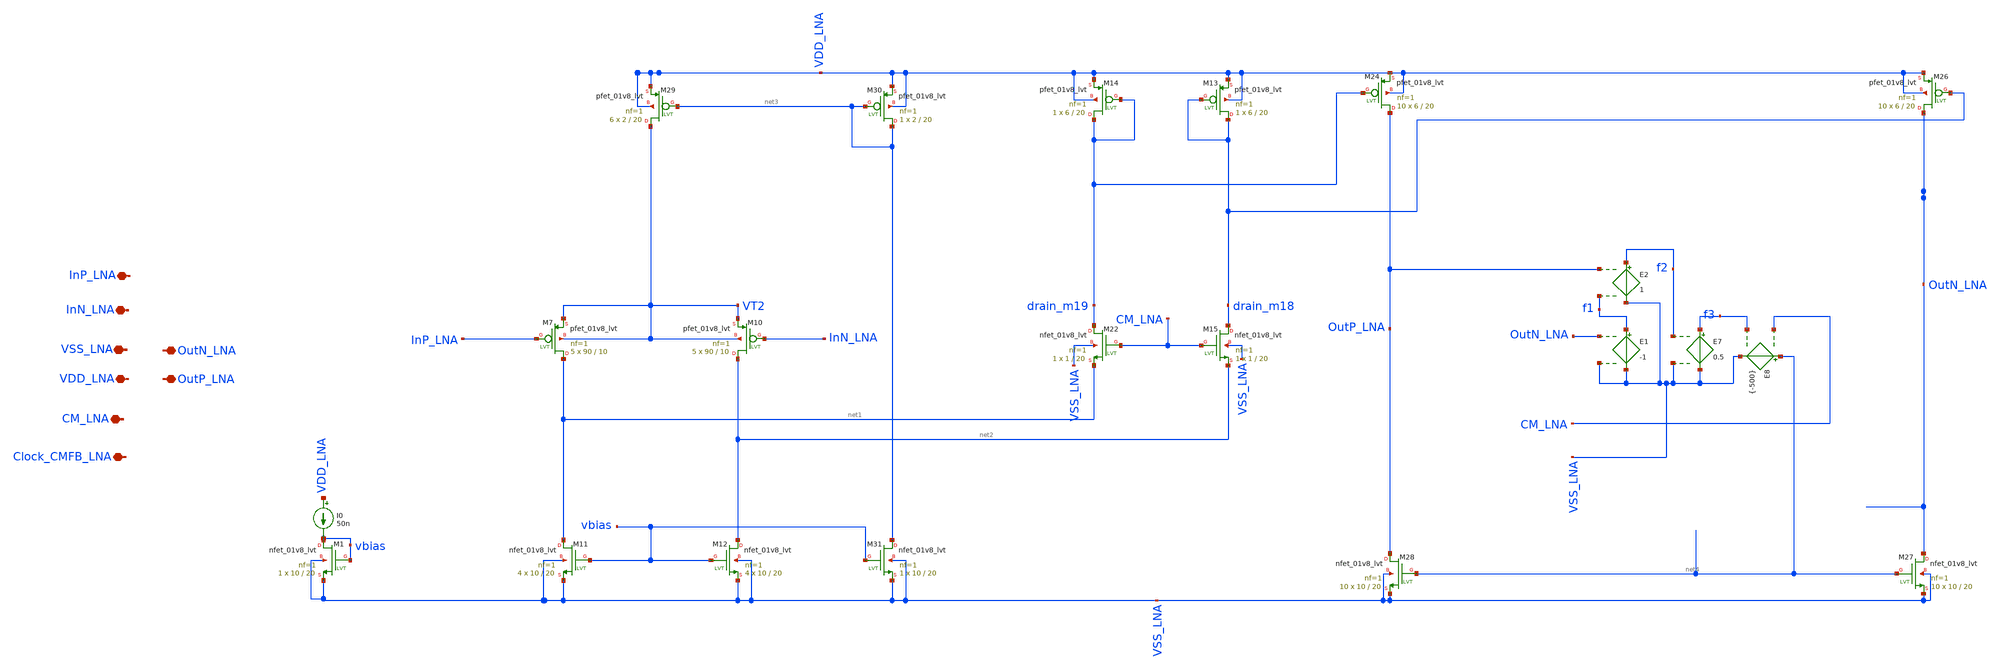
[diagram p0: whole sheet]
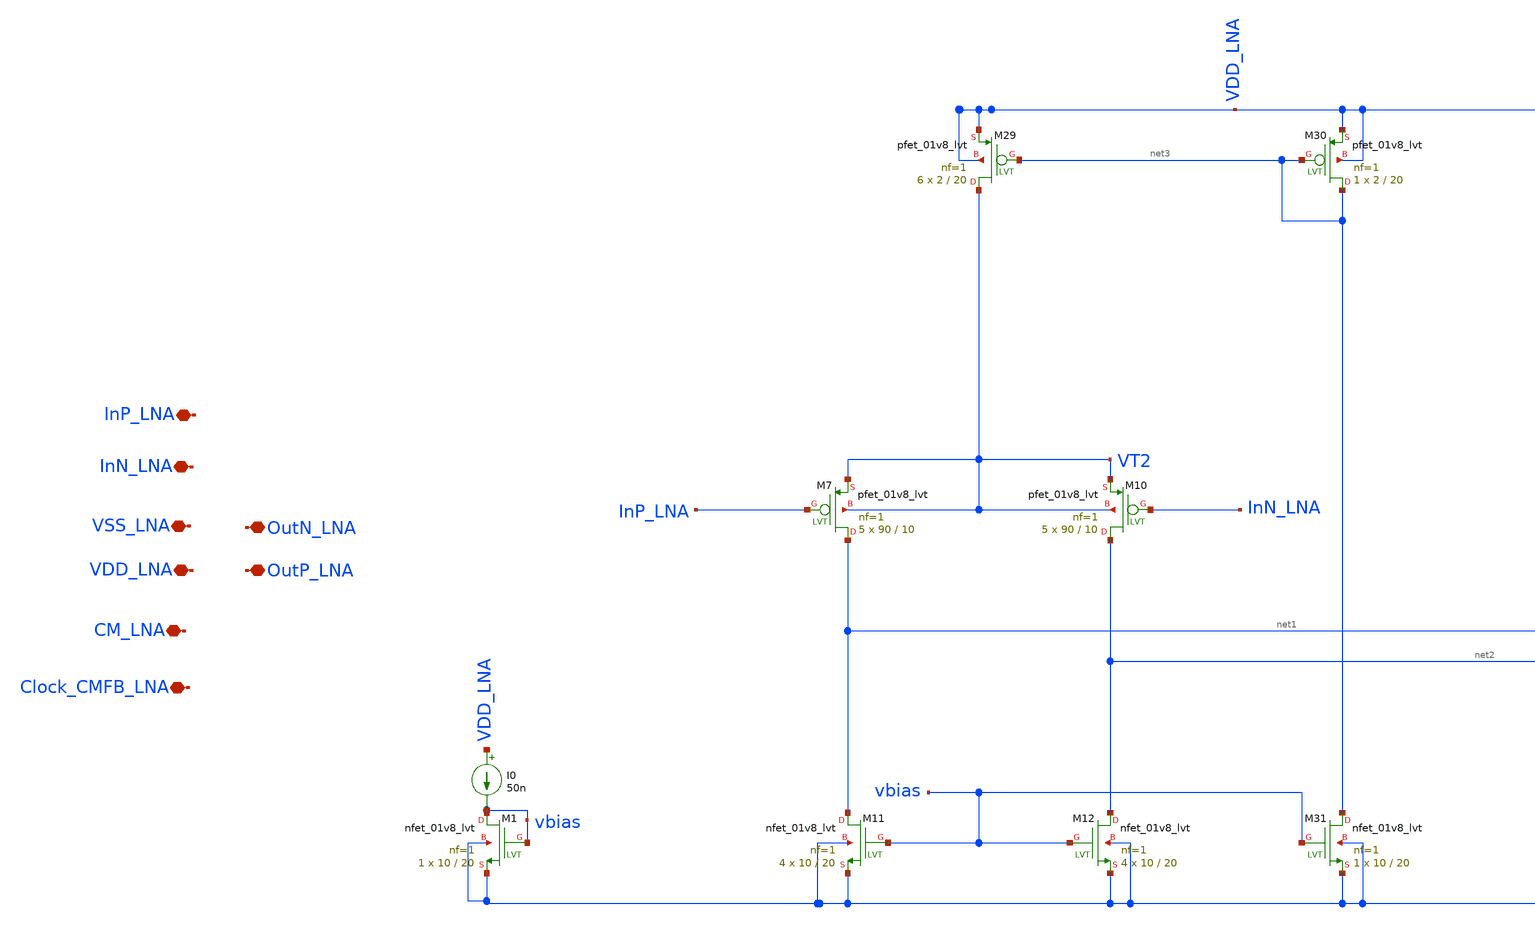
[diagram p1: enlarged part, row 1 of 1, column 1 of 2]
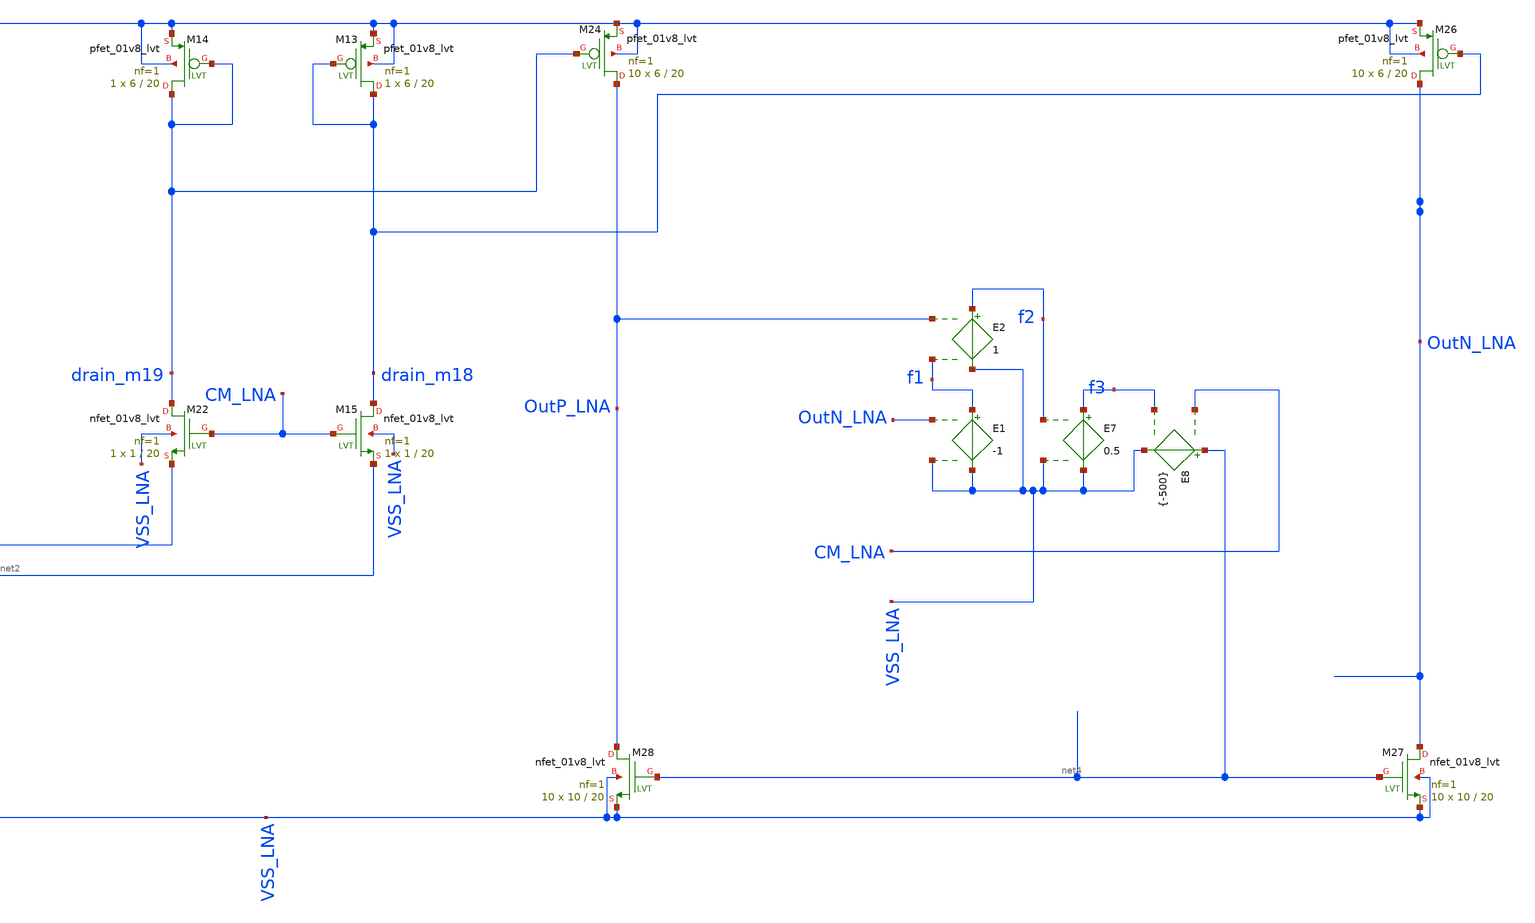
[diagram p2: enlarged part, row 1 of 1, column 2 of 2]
** sch_path: LNA_ac.sch
**.subckt LNA_ac InP_LNA InN_LNA VSS_LNA VDD_LNA CM_LNA OutP_LNA OutN_LNA Clock_CMFB_LNA
*.iopin InP_LNA
*.iopin InN_LNA
*.iopin VSS_LNA
*.iopin VDD_LNA
*.iopin CM_LNA
*.iopin OutP_LNA
*.iopin OutN_LNA
*.iopin Clock_CMFB_LNA
XM7 net1 InP_LNA VT2 VT2 sky130_fd_pr__pfet_01v8_lvt L=10 W=90 nf=1 ad='int((nf+1)/2) * W/nf * 0.29'
+ as='int((nf+2)/2) * W/nf * 0.29' pd='2*int((nf+1)/2) * (W/nf + 0.29)' ps='2*int((nf+2)/2) * (W/nf + 0.29)'
+ nrd='0.29 / W' nrs='0.29 / W' sa=0 sb=0 sd=0 mult=5 m=5
XM10 net2 InN_LNA VT2 VT2 sky130_fd_pr__pfet_01v8_lvt L=10 W=90 nf=1 ad='int((nf+1)/2) * W/nf * 0.29'
+ as='int((nf+2)/2) * W/nf * 0.29' pd='2*int((nf+1)/2) * (W/nf + 0.29)' ps='2*int((nf+2)/2) * (W/nf + 0.29)'
+ nrd='0.29 / W' nrs='0.29 / W' sa=0 sb=0 sd=0 mult=5 m=5
XM11 net1 vbias VSS_LNA VSS_LNA sky130_fd_pr__nfet_01v8_lvt L=20 W=10 nf=1 ad='int((nf+1)/2) * W/nf * 0.29'
+ as='int((nf+2)/2) * W/nf * 0.29' pd='2*int((nf+1)/2) * (W/nf + 0.29)' ps='2*int((nf+2)/2) * (W/nf + 0.29)'
+ nrd='0.29 / W' nrs='0.29 / W' sa=0 sb=0 sd=0 mult=4 m=4
XM12 net2 vbias VSS_LNA VSS_LNA sky130_fd_pr__nfet_01v8_lvt L=20 W=10 nf=1 ad='int((nf+1)/2) * W/nf * 0.29'
+ as='int((nf+2)/2) * W/nf * 0.29' pd='2*int((nf+1)/2) * (W/nf + 0.29)' ps='2*int((nf+2)/2) * (W/nf + 0.29)'
+ nrd='0.29 / W' nrs='0.29 / W' sa=0 sb=0 sd=0 mult=4 m=4
XM13 drain_m18 drain_m18 VDD_LNA VDD_LNA sky130_fd_pr__pfet_01v8_lvt L=20 W=6 nf=1 ad='int((nf+1)/2) * W/nf * 0.29'
+ as='int((nf+2)/2) * W/nf * 0.29' pd='2*int((nf+1)/2) * (W/nf + 0.29)' ps='2*int((nf+2)/2) * (W/nf + 0.29)'
+ nrd='0.29 / W' nrs='0.29 / W' sa=0 sb=0 sd=0 mult=1 m=1
XM14 drain_m19 drain_m19 VDD_LNA VDD_LNA sky130_fd_pr__pfet_01v8_lvt L=20 W=6 nf=1 ad='int((nf+1)/2) * W/nf * 0.29'
+ as='int((nf+2)/2) * W/nf * 0.29' pd='2*int((nf+1)/2) * (W/nf + 0.29)' ps='2*int((nf+2)/2) * (W/nf + 0.29)'
+ nrd='0.29 / W' nrs='0.29 / W' sa=0 sb=0 sd=0 mult=1 m=1
XM15 drain_m18 CM_LNA net2 VSS_LNA sky130_fd_pr__nfet_01v8_lvt L=20 W=1 nf=1 ad='int((nf+1)/2) * W/nf * 0.29'
+ as='int((nf+2)/2) * W/nf * 0.29' pd='2*int((nf+1)/2) * (W/nf + 0.29)' ps='2*int((nf+2)/2) * (W/nf + 0.29)'
+ nrd='0.29 / W' nrs='0.29 / W' sa=0 sb=0 sd=0 mult=1 m=1
XM22 drain_m19 CM_LNA net1 VSS_LNA sky130_fd_pr__nfet_01v8_lvt L=20 W=1 nf=1 ad='int((nf+1)/2) * W/nf * 0.29'
+ as='int((nf+2)/2) * W/nf * 0.29' pd='2*int((nf+1)/2) * (W/nf + 0.29)' ps='2*int((nf+2)/2) * (W/nf + 0.29)'
+ nrd='0.29 / W' nrs='0.29 / W' sa=0 sb=0 sd=0 mult=1 m=1
XM24 OutP_LNA drain_m19 VDD_LNA VDD_LNA sky130_fd_pr__pfet_01v8_lvt L=20 W=6 nf=1 ad='int((nf+1)/2) * W/nf * 0.29'
+ as='int((nf+2)/2) * W/nf * 0.29' pd='2*int((nf+1)/2) * (W/nf + 0.29)' ps='2*int((nf+2)/2) * (W/nf + 0.29)'
+ nrd='0.29 / W' nrs='0.29 / W' sa=0 sb=0 sd=0 mult=10 m=10
XM26 OutN_LNA drain_m18 VDD_LNA VDD_LNA sky130_fd_pr__pfet_01v8_lvt L=20 W=6 nf=1 ad='int((nf+1)/2) * W/nf * 0.29'
+ as='int((nf+2)/2) * W/nf * 0.29' pd='2*int((nf+1)/2) * (W/nf + 0.29)' ps='2*int((nf+2)/2) * (W/nf + 0.29)'
+ nrd='0.29 / W' nrs='0.29 / W' sa=0 sb=0 sd=0 mult=10 m=10
XM27 OutN_LNA net4 VSS_LNA VSS_LNA sky130_fd_pr__nfet_01v8_lvt L=20 W=10 nf=1 ad='int((nf+1)/2) * W/nf * 0.29'
+ as='int((nf+2)/2) * W/nf * 0.29' pd='2*int((nf+1)/2) * (W/nf + 0.29)' ps='2*int((nf+2)/2) * (W/nf + 0.29)'
+ nrd='0.29 / W' nrs='0.29 / W' sa=0 sb=0 sd=0 mult=10 m=10
XM28 OutP_LNA net4 VSS_LNA VSS_LNA sky130_fd_pr__nfet_01v8_lvt L=20 W=10 nf=1 ad='int((nf+1)/2) * W/nf * 0.29'
+ as='int((nf+2)/2) * W/nf * 0.29' pd='2*int((nf+1)/2) * (W/nf + 0.29)' ps='2*int((nf+2)/2) * (W/nf + 0.29)'
+ nrd='0.29 / W' nrs='0.29 / W' sa=0 sb=0 sd=0 mult=10 m=10
XM29 VT2 net3 VDD_LNA VDD_LNA sky130_fd_pr__pfet_01v8_lvt L=20 W=2 nf=1 ad='int((nf+1)/2) * W/nf * 0.29'
+ as='int((nf+2)/2) * W/nf * 0.29' pd='2*int((nf+1)/2) * (W/nf + 0.29)' ps='2*int((nf+2)/2) * (W/nf + 0.29)'
+ nrd='0.29 / W' nrs='0.29 / W' sa=0 sb=0 sd=0 mult=6 m=6
XM30 net3 net3 VDD_LNA VDD_LNA sky130_fd_pr__pfet_01v8_lvt L=20 W=2 nf=1 ad='int((nf+1)/2) * W/nf * 0.29'
+ as='int((nf+2)/2) * W/nf * 0.29' pd='2*int((nf+1)/2) * (W/nf + 0.29)' ps='2*int((nf+2)/2) * (W/nf + 0.29)'
+ nrd='0.29 / W' nrs='0.29 / W' sa=0 sb=0 sd=0 mult=1 m=1
XM31 net3 vbias VSS_LNA VSS_LNA sky130_fd_pr__nfet_01v8_lvt L=20 W=10 nf=1 ad='int((nf+1)/2) * W/nf * 0.29'
+ as='int((nf+2)/2) * W/nf * 0.29' pd='2*int((nf+1)/2) * (W/nf + 0.29)' ps='2*int((nf+2)/2) * (W/nf + 0.29)'
+ nrd='0.29 / W' nrs='0.29 / W' sa=0 sb=0 sd=0 mult=1 m=1
E1 f1 VSS_LNA OutN_LNA VSS_LNA -1
E2 f2 VSS_LNA OutP_LNA f1 1
E7 f3 VSS_LNA f2 VSS_LNA 0.5
E8 net4 VSS_LNA CM_LNA f3 {-500}
XM1 vbias vbias VSS_LNA VSS_LNA sky130_fd_pr__nfet_01v8_lvt L=20 W=10 nf=1 ad='int((nf+1)/2) * W/nf * 0.29'
+ as='int((nf+2)/2) * W/nf * 0.29' pd='2*int((nf+1)/2) * (W/nf + 0.29)' ps='2*int((nf+2)/2) * (W/nf + 0.29)'
+ nrd='0.29 / W' nrs='0.29 / W' sa=0 sb=0 sd=0 mult=1 m=1
I0 VDD_LNA vbias 50n
**.ends
.end
